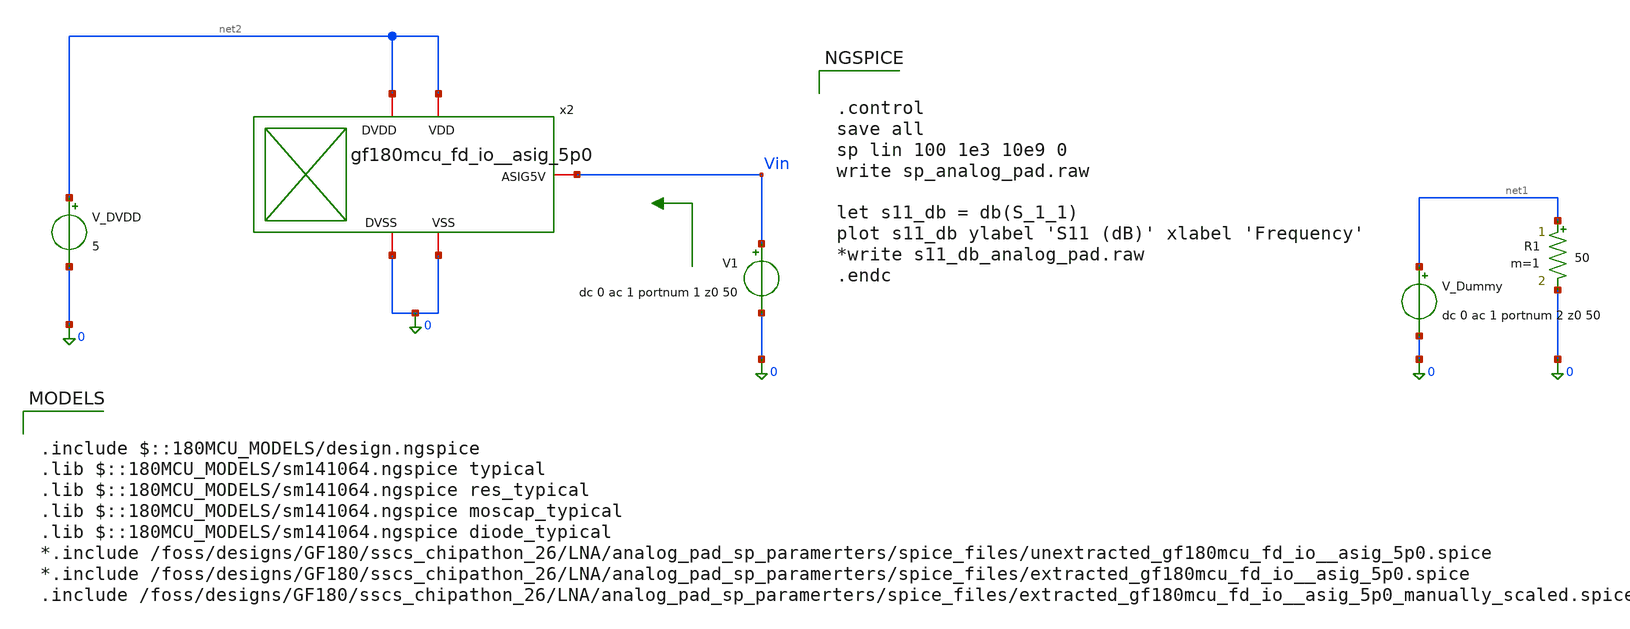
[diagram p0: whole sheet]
** sch_path: analog_pad_sp_paramerters/xschem/schematic_sp.sch
**.subckt schematic_sp
V1 Vin 0 dc 0 ac 1 portnum 1 z0 50
V_DVDD net2 0 5
V_Dummy net1 0 dc 0 ac 1 portnum 2 z0 50
R1 net1 0 50 m=1
x2 net2 Vin 0 net2 0 gf180mcu_fd_io__asig_5p0
**** begin user architecture code


.control
save all
sp lin 100 1e3 10e9 0
write sp_analog_pad.raw

let s11_db = db(S_1_1)
plot s11_db ylabel 'S11 (dB)' xlabel 'Frequency'
*write s11_db_analog_pad.raw
.endc



.include $::180MCU_MODELS/design.ngspice
.lib $::180MCU_MODELS/sm141064.ngspice typical
.lib $::180MCU_MODELS/sm141064.ngspice res_typical
.lib $::180MCU_MODELS/sm141064.ngspice moscap_typical
.lib $::180MCU_MODELS/sm141064.ngspice diode_typical
*.include /foss/designs/GF180/sscs_chipathon_26/LNA/analog_pad_sp_paramerters/spice_files/unextracted_gf180mcu_fd_io__asig_5p0.spice
*.include /foss/designs/GF180/sscs_chipathon_26/LNA/analog_pad_sp_paramerters/spice_files/extracted_gf180mcu_fd_io__asig_5p0.spice
.include /foss/designs/GF180/sscs_chipathon_26/LNA/analog_pad_sp_paramerters/spice_files/extracted_gf180mcu_fd_io__asig_5p0_manually_scaled.spice

**** end user architecture code
**.ends
.end
